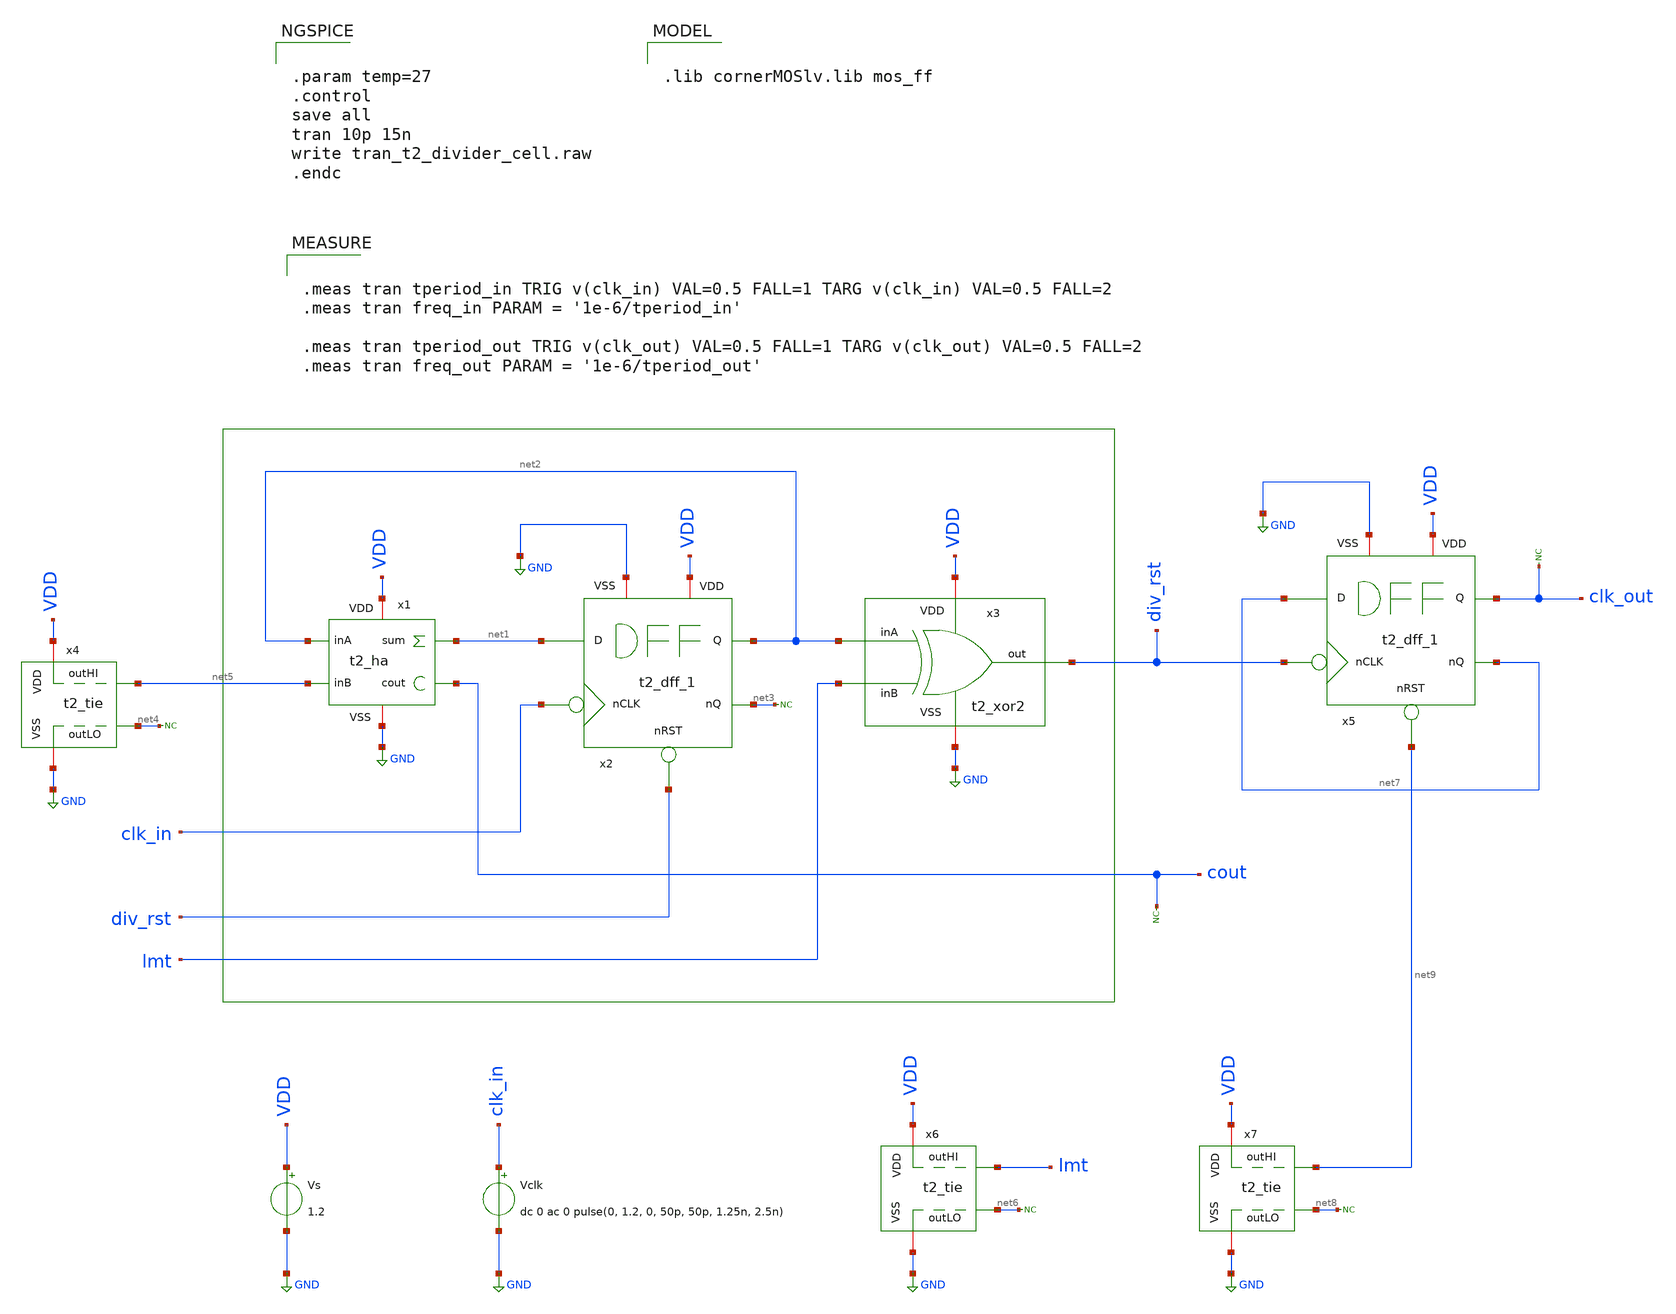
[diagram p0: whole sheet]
** sch_path: Team 2 Design/design_data/xschem/t2_divider_cell_tb.sch
**.subckt t2_divider_cell_tb
x1 VDD GND net2 net5 net1 cout t2_ha
x2 VDD GND net1 clk_in div_rst net2 net3 t2_dff_1
x3 VDD GND net2 lmt div_rst t2_xor2
* noconn #net3
x4 VDD GND net5 net4 t2_tie
* noconn #net4
Vs VDD GND 1.2
Vclk clk_in GND dc 0 ac 0 pulse(0, 1.2, 0, 50p, 50p, 1.25n, 2.5n)
x6 VDD GND lmt net6 t2_tie
* noconn #net6
* noconn cout
* noconn clk_out
x5 VDD GND net7 div_rst net9 clk_out net7 t2_dff_1
x7 VDD GND net9 net8 t2_tie
* noconn #net8
**** begin user architecture code


.param temp=27
.control
save all
tran 10p 15n
write tran_t2_divider_cell.raw
.endc



.lib cornerMOSlv.lib mos_ff



.meas tran tperiod_in TRIG v(clk_in) VAL=0.5 FALL=1 TARG v(clk_in) VAL=0.5 FALL=2
.meas tran freq_in PARAM = '1e-6/tperiod_in'

.meas tran tperiod_out TRIG v(clk_out) VAL=0.5 FALL=1 TARG v(clk_out) VAL=0.5 FALL=2
.meas tran freq_out PARAM = '1e-6/tperiod_out'


**** end user architecture code
**.ends
.GLOBAL GND
.end
